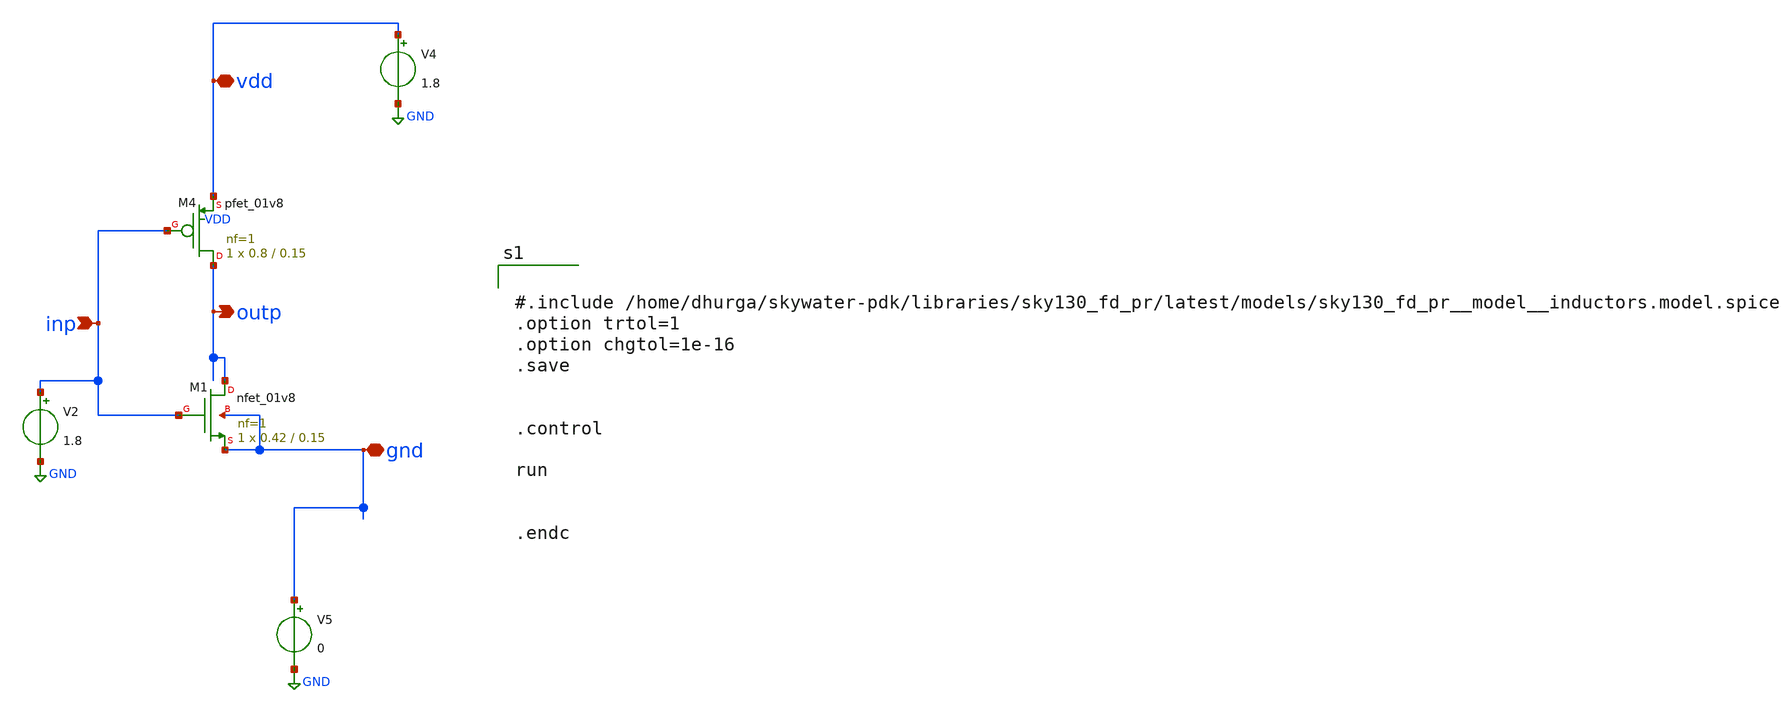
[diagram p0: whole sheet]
** sch_path: Xschem_ngspice_magic_netgen_caravel/inv_ay_xschem.sch
**.subckt inv_ay_xschem inp outp vdd gnd
*.ipin inp
*.opin outp
*.iopin vdd
*.iopin gnd
XM1 outp inp gnd gnd sky130_fd_pr__nfet_01v8 L=0.15 W=0.42 nf=1 ad='int((nf+1)/2) * W/nf * 0.29' as='int((nf+2)/2) * W/nf * 0.29'
+ pd='2*int((nf+1)/2) * (W/nf + 0.29)' ps='2*int((nf+2)/2) * (W/nf + 0.29)' nrd='0.29 / W' nrs='0.29 / W'
+ sa=0 sb=0 sd=0 mult=1 m=1
XM4 outp inp vdd VDD sky130_fd_pr__pfet_01v8 L=0.15 W=0.8 nf=1 ad='int((nf+1)/2) * W/nf * 0.29' as='int((nf+2)/2) * W/nf * 0.29'
+ pd='2*int((nf+1)/2) * (W/nf + 0.29)' ps='2*int((nf+2)/2) * (W/nf + 0.29)' nrd='0.29 / W' nrs='0.29 / W'
+ sa=0 sb=0 sd=0 mult=1 m=1
V2 inp GND 1.8
V4 vdd GND 1.8
V5 gnd GND 0
**** begin user architecture code



.lib /home/dhurga/open_pdks/sky130/sky130A/libs.tech/ngspice/sky130.lib.spice tt
#.include /home/dhurga/skywater-pdk/libraries/sky130_fd_pr/latest/models/sky130_fd_pr__model__inductors.model.spice
*.lib ~/open_pdks/sky130/sky130A/libs.tech/ngspice/sky130.lib.spice hh
* Resistor/Capacitor
*.include /home/dhurga/open_pdks/sky130/sky130A/libs.tech/ngspice/r+c/res_high__cap_high.spice
*.include /home/dhurga/open_pdks/sky130/sky130A/libs.tech/ngspice/r+c/res_high__cap_high__lin.spice
*.include /home/dhurga/open_pdks/sky130/sky130A/libs.tech/ngspice/corners/ff/specialized_cells.spice


*.include ~/open_pdks/sky130/sky130A/libs.tech/ngspice/corners/tt/nonfet.spice/wb_flat.spice



#.include /home/dhurga/skywater-pdk/libraries/sky130_fd_pr/latest/models/sky130_fd_pr__model__inductors.model.spice
.option trtol=1
.option chgtol=1e-16
.save


.control

run


.endc


**** end user architecture code
**.ends
.GLOBAL GND
.end
